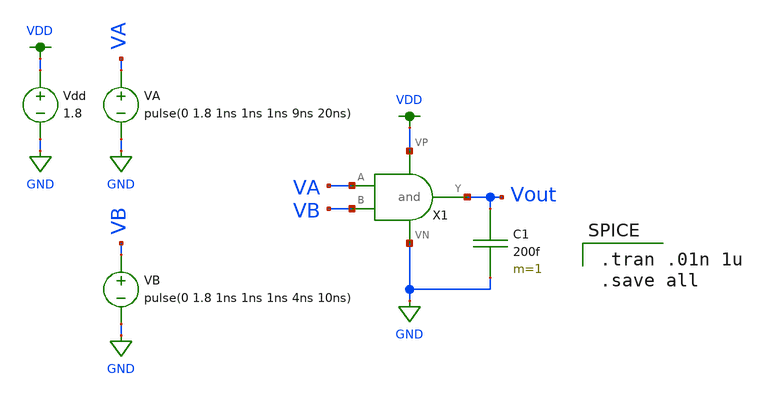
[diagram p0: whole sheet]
** sch_path: mini_proj_1/schematic/and_test.sch
**.subckt and_test
X1 VA VB VDD GND Vout and
C1 Vout GND 200f m=1
Vdd VDD GND 1.8
VA VA GND pulse(0 1.8 1ns 1ns 1ns 9ns 20ns)
VB VB GND pulse(0 1.8 1ns 1ns 1ns 4ns 10ns)
**** begin user architecture code

.option wnflag=1
.lib ~/skywater/skywater-pdk/libraries/sky130_fd_pr_ngspice/latest/models/sky130.lib.spice tt


.tran .01n 1u
.save all

**** end user architecture code
**.ends
.GLOBAL GND
.GLOBAL VDD
.end
